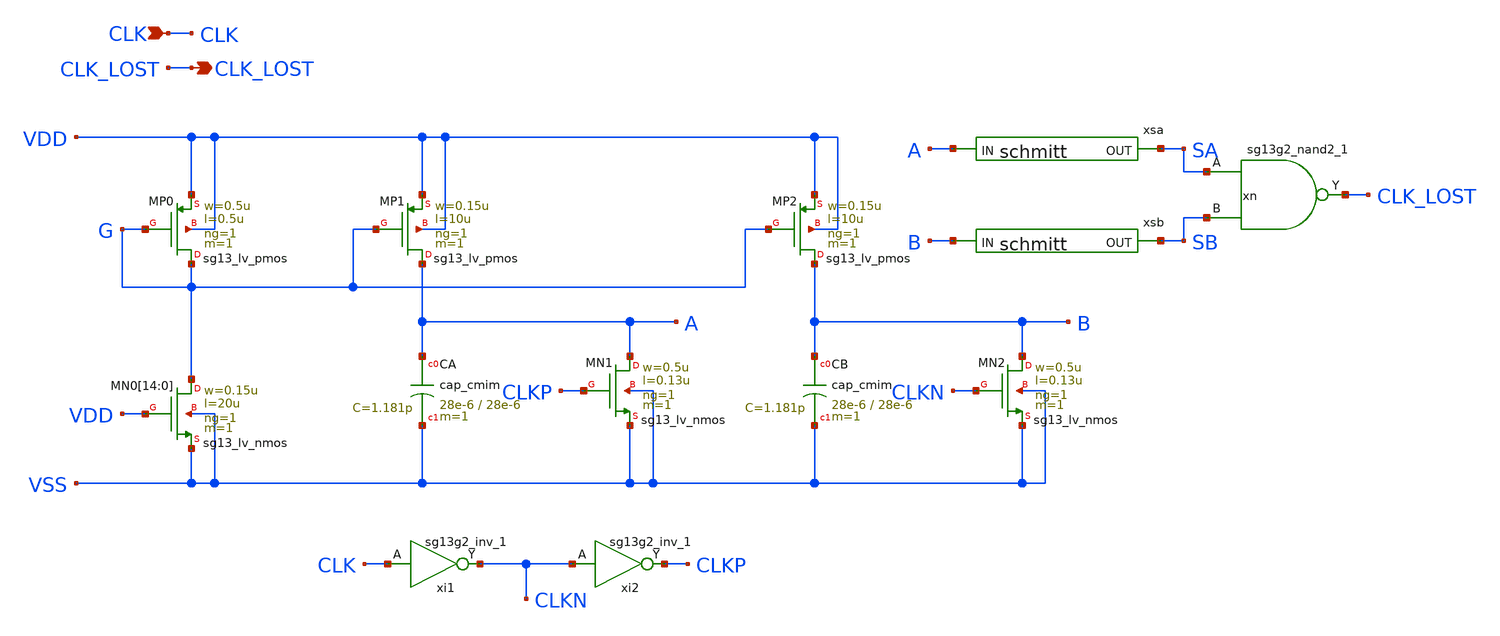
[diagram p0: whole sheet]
** sch_path: design/blocks/clkmon/schematic/wd_clkmon.sch
**.subckt wd_clkmon CLK CLK_LOST
*.ipin CLK
*.opin CLK_LOST
XMP0 G G VDD VDD sg13_lv_pmos w=0.5u l=0.5u ng=1 m=1 mm_ok=1
XMN0[14] G VDD VSS VSS sg13_lv_nmos w=0.15u l=20u ng=1 m=1 mm_ok=1
XMN0[13] G VDD VSS VSS sg13_lv_nmos w=0.15u l=20u ng=1 m=1 mm_ok=1
XMN0[12] G VDD VSS VSS sg13_lv_nmos w=0.15u l=20u ng=1 m=1 mm_ok=1
XMN0[11] G VDD VSS VSS sg13_lv_nmos w=0.15u l=20u ng=1 m=1 mm_ok=1
XMN0[10] G VDD VSS VSS sg13_lv_nmos w=0.15u l=20u ng=1 m=1 mm_ok=1
XMN0[9] G VDD VSS VSS sg13_lv_nmos w=0.15u l=20u ng=1 m=1 mm_ok=1
XMN0[8] G VDD VSS VSS sg13_lv_nmos w=0.15u l=20u ng=1 m=1 mm_ok=1
XMN0[7] G VDD VSS VSS sg13_lv_nmos w=0.15u l=20u ng=1 m=1 mm_ok=1
XMN0[6] G VDD VSS VSS sg13_lv_nmos w=0.15u l=20u ng=1 m=1 mm_ok=1
XMN0[5] G VDD VSS VSS sg13_lv_nmos w=0.15u l=20u ng=1 m=1 mm_ok=1
XMN0[4] G VDD VSS VSS sg13_lv_nmos w=0.15u l=20u ng=1 m=1 mm_ok=1
XMN0[3] G VDD VSS VSS sg13_lv_nmos w=0.15u l=20u ng=1 m=1 mm_ok=1
XMN0[2] G VDD VSS VSS sg13_lv_nmos w=0.15u l=20u ng=1 m=1 mm_ok=1
XMN0[1] G VDD VSS VSS sg13_lv_nmos w=0.15u l=20u ng=1 m=1 mm_ok=1
XMN0[0] G VDD VSS VSS sg13_lv_nmos w=0.15u l=20u ng=1 m=1 mm_ok=1
XMP1 A G VDD VDD sg13_lv_pmos w=0.15u l=10u ng=1 m=1 mm_ok=1
XCA A VSS cap_cmim w=28e-6 l=28e-6 m=1 mm_ok=1
XMN1 A CLKP VSS VSS sg13_lv_nmos w=0.5u l=0.13u ng=1 m=1 mm_ok=1
XMP2 B G VDD VDD sg13_lv_pmos w=0.15u l=10u ng=1 m=1 mm_ok=1
XCB B VSS cap_cmim w=28e-6 l=28e-6 m=1 mm_ok=1
XMN2 B CLKN VSS VSS sg13_lv_nmos w=0.5u l=0.13u ng=1 m=1 mm_ok=1
xi1 CLKN CLK VDD VSS sg13g2_inv_1
xi2 CLKP CLKN VDD VSS sg13g2_inv_1
xsa A SA VDD VSS schmitt
xsb B SB VDD VSS schmitt
xn CLK_LOST SA SB VDD VSS sg13g2_nand2_1
**.ends

* expanding   symbol:  sg13g2_inv_1.sym # of pins=2
** sym_path: sg13g2_inv_1.sym
** sch_path: sg13g2_inv_1.sch
.subckt sg13g2_inv_1 Y A VDD VSS
*.opin Y
*.ipin A
*.iopin VDD
*.iopin VSS
XM1 Y A VSS VSS sg13_lv_nmos w=740.00n l=130.00n ng=1 m=1 mm_ok=1
XM2 Y A VDD VDD sg13_lv_pmos w=1.12u l=130.00n ng=1 m=1 mm_ok=1
.ends


* expanding   symbol:  schmitt.sym # of pins=2
** sym_path: design/blocks/schmitt/schematic/schmitt.sym
** sch_path: design/blocks/schmitt/schematic/schmitt.sch
.subckt schmitt IN OUT VDD VSS
*.opin OUT
*.ipin IN
XM4 net1 IN VDD VDD sg13_lv_pmos w=1.04u l=0.13u ng=1 m=1 mm_ok=1
XM6 OUT IN net2 VSS sg13_lv_nmos w=0.76u l=0.13u ng=1 m=1 mm_ok=1
XM5 OUT IN net1 VDD sg13_lv_pmos w=1.04u l=0.13u ng=1 m=1 mm_ok=1
XM7 net2 IN VSS VSS sg13_lv_nmos w=0.76u l=0.13u ng=1 m=1 mm_ok=1
XM8 VSS OUT net1 VDD sg13_lv_pmos w=0.42u l=0.13u ng=1 m=1 mm_ok=1
XM9 VDD OUT net2 VSS sg13_lv_nmos w=0.42u l=0.13u ng=1 m=1 mm_ok=1
.ends


* expanding   symbol:  sg13g2_nand2_1.sym # of pins=3
** sym_path: sg13g2_nand2_1.sym
** sch_path: sg13g2_nand2_1.sch
.subckt sg13g2_nand2_1 Y A B VDD VSS
*.iopin VDD
*.iopin VSS
*.ipin A
*.ipin B
*.opin Y
XM1 Y A net1 VSS sg13_lv_nmos w=740.00n l=130.00n ng=1 m=1 mm_ok=1
XM2 net1 B VSS VSS sg13_lv_nmos w=740.00n l=130.00n ng=1 m=1 mm_ok=1
XM3 Y A VDD VDD sg13_lv_pmos w=1.12u l=130.00n ng=1 m=1 mm_ok=1
XM4 Y B VDD VDD sg13_lv_pmos w=1.12u l=130.00n ng=1 m=1 mm_ok=1
.ends

.end
